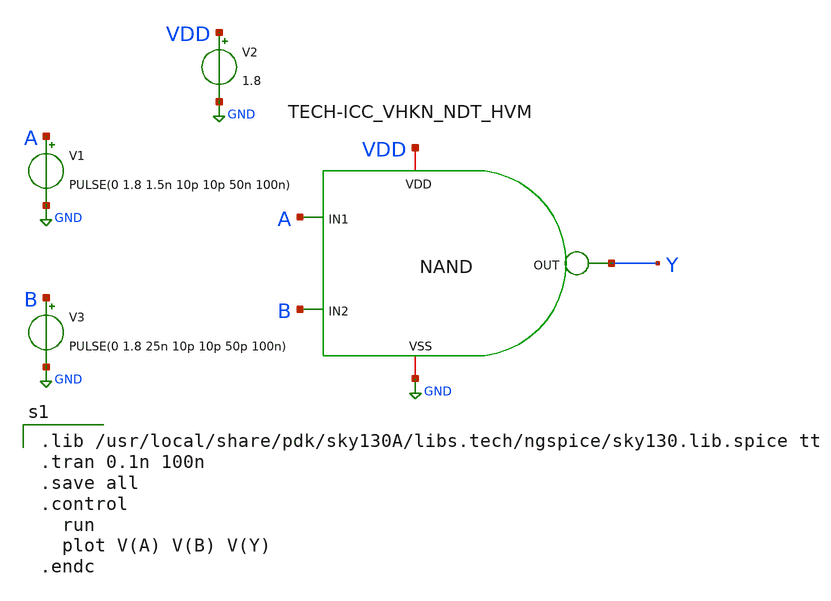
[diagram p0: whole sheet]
** sch_path: DECODER3TO8/Schematic/CMOS_NAND_SCHEMATIC.sch
**.subckt CMOS_NAND_SCHEMATIC
V1 A GND PULSE(0 1.8 1.5n 10p 10p 50n 100n)
V2 VDD GND 1.8
V3 B GND PULSE(0 1.8 25n 10p 10p 50p 100n)
x1 VDD Y A B GND NAND
**** begin user architecture code

.lib /usr/local/share/pdk/sky130A/libs.tech/ngspice/sky130.lib.spice tt
.tran 0.1n 100n
.save all
.control
  run
  plot V(A) V(B) V(Y)
.endc


**** end user architecture code
**.ends
.GLOBAL GND
.end
